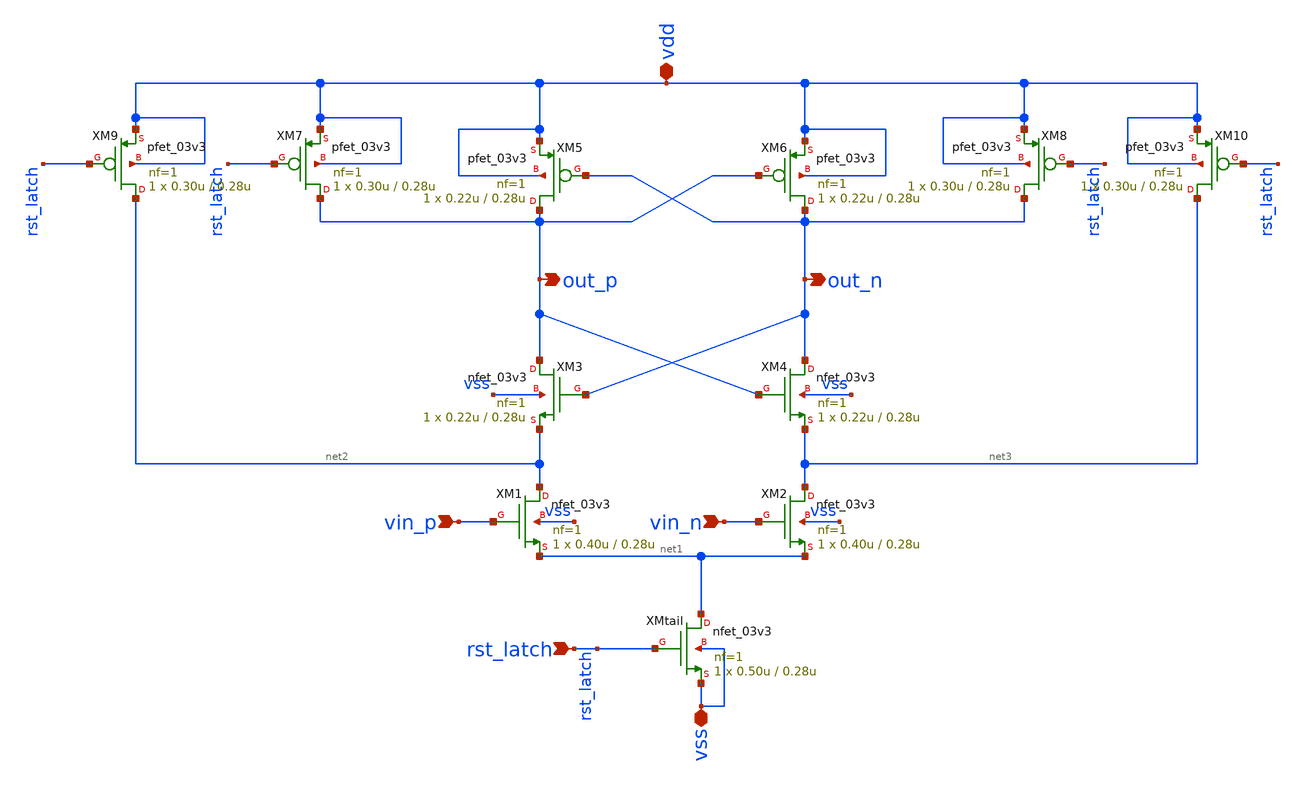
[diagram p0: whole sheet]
** sch_path: xschem/sar_adc/blocks/comparator/strongarm_comp_core.sch
**.subckt strongarm_comp_core vin_p vin_n rst_latch vdd vss out_p out_n
*.ipin vin_p
*.ipin vin_n
*.ipin rst_latch
*.iopin vdd
*.iopin vss
*.opin out_p
*.opin out_n
XMtail net1 rst_latch vss vss nfet_03v3 L=0.28u W=0.50u nf=1 ad='int((nf+1)/2) * W/nf * 0.18u' as='int((nf+2)/2) * W/nf * 0.18u'
+ pd='2*int((nf+1)/2) * (W/nf + 0.18u)' ps='2*int((nf+2)/2) * (W/nf + 0.18u)' nrd='0.18u / W' nrs='0.18u / W'
+ sa=0 sb=0 sd=0 m=1
XM1 net2 vin_p net1 vss nfet_03v3 L=0.28u W=0.40u nf=1 ad='int((nf+1)/2) * W/nf * 0.18u' as='int((nf+2)/2) * W/nf * 0.18u'
+ pd='2*int((nf+1)/2) * (W/nf + 0.18u)' ps='2*int((nf+2)/2) * (W/nf + 0.18u)' nrd='0.18u / W' nrs='0.18u / W'
+ sa=0 sb=0 sd=0 m=1
XM2 net3 vin_n net1 vss nfet_03v3 L=0.28u W=0.40u nf=1 ad='int((nf+1)/2) * W/nf * 0.18u' as='int((nf+2)/2) * W/nf * 0.18u'
+ pd='2*int((nf+1)/2) * (W/nf + 0.18u)' ps='2*int((nf+2)/2) * (W/nf + 0.18u)' nrd='0.18u / W' nrs='0.18u / W'
+ sa=0 sb=0 sd=0 m=1
XM3 out_p out_n net2 vss nfet_03v3 L=0.28u W=0.22u nf=1 ad='int((nf+1)/2) * W/nf * 0.18u' as='int((nf+2)/2) * W/nf * 0.18u'
+ pd='2*int((nf+1)/2) * (W/nf + 0.18u)' ps='2*int((nf+2)/2) * (W/nf + 0.18u)' nrd='0.18u / W' nrs='0.18u / W'
+ sa=0 sb=0 sd=0 m=1
XM4 out_n out_p net3 vss nfet_03v3 L=0.28u W=0.22u nf=1 ad='int((nf+1)/2) * W/nf * 0.18u' as='int((nf+2)/2) * W/nf * 0.18u'
+ pd='2*int((nf+1)/2) * (W/nf + 0.18u)' ps='2*int((nf+2)/2) * (W/nf + 0.18u)' nrd='0.18u / W' nrs='0.18u / W'
+ sa=0 sb=0 sd=0 m=1
XM5 out_p out_n vdd vdd pfet_03v3 L=0.28u W=0.22u nf=1 ad='int((nf+1)/2) * W/nf * 0.18u' as='int((nf+2)/2) * W/nf * 0.18u'
+ pd='2*int((nf+1)/2) * (W/nf + 0.18u)' ps='2*int((nf+2)/2) * (W/nf + 0.18u)' nrd='0.18u / W' nrs='0.18u / W'
+ sa=0 sb=0 sd=0 m=1
XM6 out_n out_p vdd vdd pfet_03v3 L=0.28u W=0.22u nf=1 ad='int((nf+1)/2) * W/nf * 0.18u' as='int((nf+2)/2) * W/nf * 0.18u'
+ pd='2*int((nf+1)/2) * (W/nf + 0.18u)' ps='2*int((nf+2)/2) * (W/nf + 0.18u)' nrd='0.18u / W' nrs='0.18u / W'
+ sa=0 sb=0 sd=0 m=1
XM7 out_p rst_latch vdd vdd pfet_03v3 L=0.28u W=0.30u nf=1 ad='int((nf+1)/2) * W/nf * 0.18u' as='int((nf+2)/2) * W/nf * 0.18u'
+ pd='2*int((nf+1)/2) * (W/nf + 0.18u)' ps='2*int((nf+2)/2) * (W/nf + 0.18u)' nrd='0.18u / W' nrs='0.18u / W'
+ sa=0 sb=0 sd=0 m=1
XM8 out_n rst_latch vdd vdd pfet_03v3 L=0.28u W=0.30u nf=1 ad='int((nf+1)/2) * W/nf * 0.18u' as='int((nf+2)/2) * W/nf * 0.18u'
+ pd='2*int((nf+1)/2) * (W/nf + 0.18u)' ps='2*int((nf+2)/2) * (W/nf + 0.18u)' nrd='0.18u / W' nrs='0.18u / W'
+ sa=0 sb=0 sd=0 m=1
XM9 net2 rst_latch vdd vdd pfet_03v3 L=0.28u W=0.30u nf=1 ad='int((nf+1)/2) * W/nf * 0.18u' as='int((nf+2)/2) * W/nf * 0.18u'
+ pd='2*int((nf+1)/2) * (W/nf + 0.18u)' ps='2*int((nf+2)/2) * (W/nf + 0.18u)' nrd='0.18u / W' nrs='0.18u / W'
+ sa=0 sb=0 sd=0 m=1
XM10 net3 rst_latch vdd vdd pfet_03v3 L=0.28u W=0.30u nf=1 ad='int((nf+1)/2) * W/nf * 0.18u' as='int((nf+2)/2) * W/nf * 0.18u'
+ pd='2*int((nf+1)/2) * (W/nf + 0.18u)' ps='2*int((nf+2)/2) * (W/nf + 0.18u)' nrd='0.18u / W' nrs='0.18u / W'
+ sa=0 sb=0 sd=0 m=1
**.ends
.end
